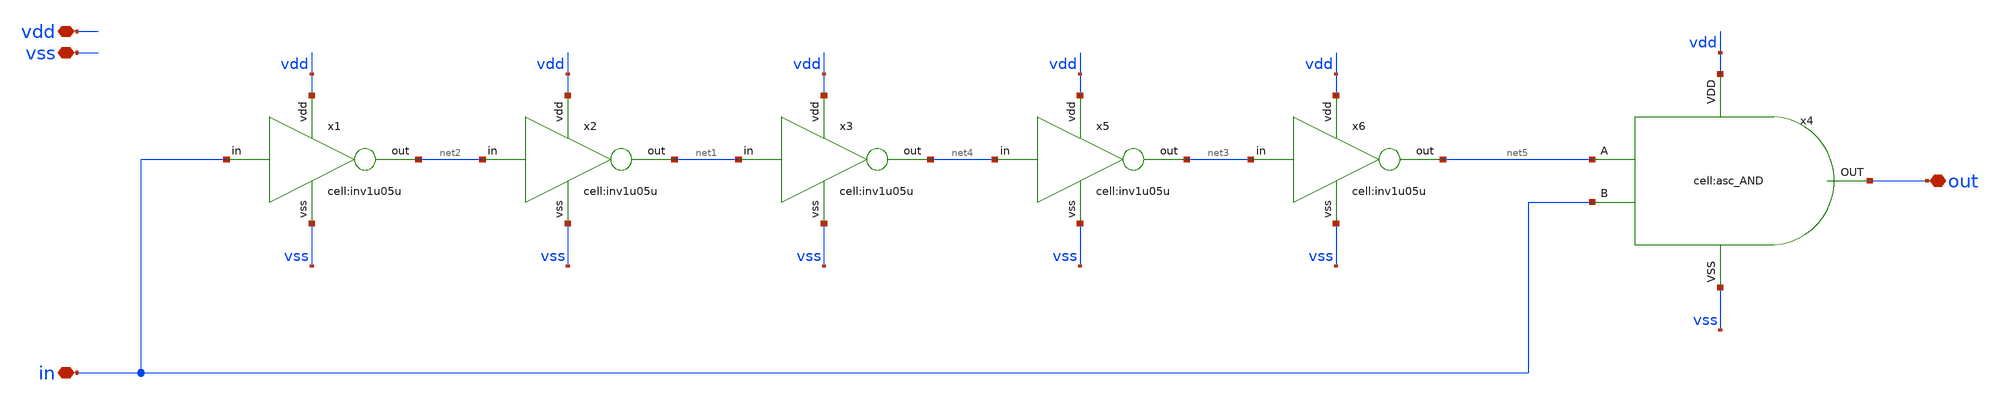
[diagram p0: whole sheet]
** sch_path: designs/libs/xp_core_analog/asc_re_pulse_detector/asc_re_pulse_detector.sch
**.subckt asc_re_pulse_detector vdd vss in out
*.iopin vdd
*.iopin vss
*.iopin in
*.iopin out
x1 in vdd net2 vss inv1u05u
x2 net2 vdd net1 vss inv1u05u
x3 net1 vdd net4 vss inv1u05u
x4 vdd out net5 in vss asc_AND
x5 net4 vdd net3 vss inv1u05u
x6 net3 vdd net5 vss inv1u05u
**.ends
.end
